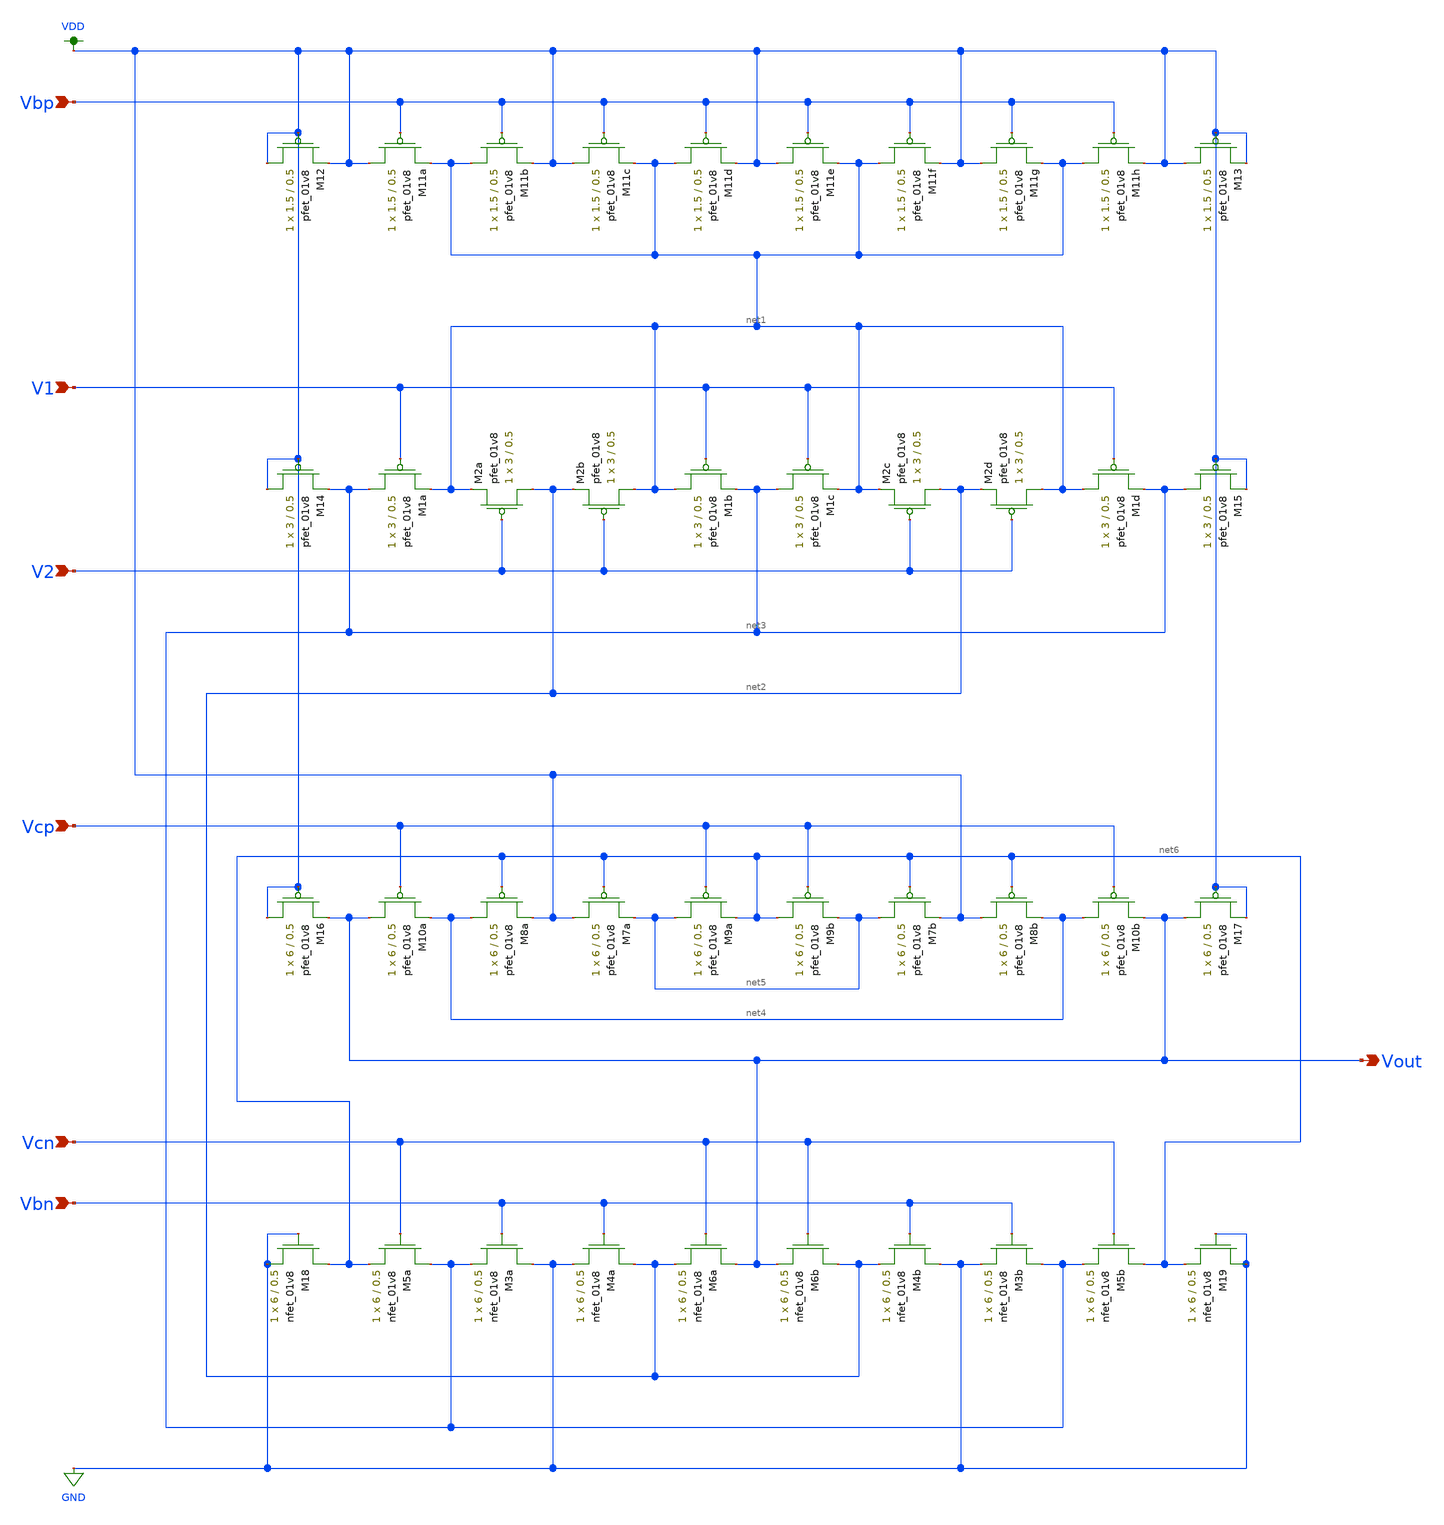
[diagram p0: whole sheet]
** sch_path: schematic/lvs_schematic/differential_pair_xschem.sch
**.subckt differential_pair_xschem Vbn Vcn Vcp V2 V1 Vbp Vout
*.ipin Vbn
*.ipin Vcn
*.ipin Vcp
*.ipin V2
*.ipin V1
*.ipin Vbp
*.opin Vout
XM5a net3 Vcn net6 GND sky130_fd_pr__nfet_01v8 L=0.5 W=6 nf=1 ad='int((nf+1)/2) * W/nf * 0.29' as='int((nf+2)/2) * W/nf * 0.29'
+ pd='2*int((nf+1)/2) * (W/nf + 0.29)' ps='2*int((nf+2)/2) * (W/nf + 0.29)' nrd='0.29 / W' nrs='0.29 / W'
+ sa=0 sb=0 sd=0 mult=1 m=1
XM1a net3 V1 net1 VDD sky130_fd_pr__pfet_01v8 L=0.5 W=3 nf=1 ad='int((nf+1)/2) * W/nf * 0.29' as='int((nf+2)/2) * W/nf * 0.29'
+ pd='2*int((nf+1)/2) * (W/nf + 0.29)' ps='2*int((nf+2)/2) * (W/nf + 0.29)' nrd='0.29 / W' nrs='0.29 / W'
+ sa=0 sb=0 sd=0 mult=1 m=1
XM2a net2 V2 net1 VDD sky130_fd_pr__pfet_01v8 L=0.5 W=3 nf=1 ad='int((nf+1)/2) * W/nf * 0.29' as='int((nf+2)/2) * W/nf * 0.29'
+ pd='2*int((nf+1)/2) * (W/nf + 0.29)' ps='2*int((nf+2)/2) * (W/nf + 0.29)' nrd='0.29 / W' nrs='0.29 / W'
+ sa=0 sb=0 sd=0 mult=1 m=1
XM2b net1 V2 net2 VDD sky130_fd_pr__pfet_01v8 L=0.5 W=3 nf=1 ad='int((nf+1)/2) * W/nf * 0.29' as='int((nf+2)/2) * W/nf * 0.29'
+ pd='2*int((nf+1)/2) * (W/nf + 0.29)' ps='2*int((nf+2)/2) * (W/nf + 0.29)' nrd='0.29 / W' nrs='0.29 / W'
+ sa=0 sb=0 sd=0 mult=1 m=1
XM1b net1 V1 net3 VDD sky130_fd_pr__pfet_01v8 L=0.5 W=3 nf=1 ad='int((nf+1)/2) * W/nf * 0.29' as='int((nf+2)/2) * W/nf * 0.29'
+ pd='2*int((nf+1)/2) * (W/nf + 0.29)' ps='2*int((nf+2)/2) * (W/nf + 0.29)' nrd='0.29 / W' nrs='0.29 / W'
+ sa=0 sb=0 sd=0 mult=1 m=1
XM1c net3 V1 net1 VDD sky130_fd_pr__pfet_01v8 L=0.5 W=3 nf=1 ad='int((nf+1)/2) * W/nf * 0.29' as='int((nf+2)/2) * W/nf * 0.29'
+ pd='2*int((nf+1)/2) * (W/nf + 0.29)' ps='2*int((nf+2)/2) * (W/nf + 0.29)' nrd='0.29 / W' nrs='0.29 / W'
+ sa=0 sb=0 sd=0 mult=1 m=1
XM2c net2 V2 net1 VDD sky130_fd_pr__pfet_01v8 L=0.5 W=3 nf=1 ad='int((nf+1)/2) * W/nf * 0.29' as='int((nf+2)/2) * W/nf * 0.29'
+ pd='2*int((nf+1)/2) * (W/nf + 0.29)' ps='2*int((nf+2)/2) * (W/nf + 0.29)' nrd='0.29 / W' nrs='0.29 / W'
+ sa=0 sb=0 sd=0 mult=1 m=1
XM2d net1 V2 net2 VDD sky130_fd_pr__pfet_01v8 L=0.5 W=3 nf=1 ad='int((nf+1)/2) * W/nf * 0.29' as='int((nf+2)/2) * W/nf * 0.29'
+ pd='2*int((nf+1)/2) * (W/nf + 0.29)' ps='2*int((nf+2)/2) * (W/nf + 0.29)' nrd='0.29 / W' nrs='0.29 / W'
+ sa=0 sb=0 sd=0 mult=1 m=1
XM1d net1 V1 net3 VDD sky130_fd_pr__pfet_01v8 L=0.5 W=3 nf=1 ad='int((nf+1)/2) * W/nf * 0.29' as='int((nf+2)/2) * W/nf * 0.29'
+ pd='2*int((nf+1)/2) * (W/nf + 0.29)' ps='2*int((nf+2)/2) * (W/nf + 0.29)' nrd='0.29 / W' nrs='0.29 / W'
+ sa=0 sb=0 sd=0 mult=1 m=1
XM11a VDD Vbp net1 VDD sky130_fd_pr__pfet_01v8 L=0.5 W=1.5 nf=1 ad='int((nf+1)/2) * W/nf * 0.29' as='int((nf+2)/2) * W/nf * 0.29'
+ pd='2*int((nf+1)/2) * (W/nf + 0.29)' ps='2*int((nf+2)/2) * (W/nf + 0.29)' nrd='0.29 / W' nrs='0.29 / W'
+ sa=0 sb=0 sd=0 mult=1 m=1
XM11b net1 Vbp VDD VDD sky130_fd_pr__pfet_01v8 L=0.5 W=1.5 nf=1 ad='int((nf+1)/2) * W/nf * 0.29' as='int((nf+2)/2) * W/nf * 0.29'
+ pd='2*int((nf+1)/2) * (W/nf + 0.29)' ps='2*int((nf+2)/2) * (W/nf + 0.29)' nrd='0.29 / W' nrs='0.29 / W'
+ sa=0 sb=0 sd=0 mult=1 m=1
XM11c VDD Vbp net1 VDD sky130_fd_pr__pfet_01v8 L=0.5 W=1.5 nf=1 ad='int((nf+1)/2) * W/nf * 0.29' as='int((nf+2)/2) * W/nf * 0.29'
+ pd='2*int((nf+1)/2) * (W/nf + 0.29)' ps='2*int((nf+2)/2) * (W/nf + 0.29)' nrd='0.29 / W' nrs='0.29 / W'
+ sa=0 sb=0 sd=0 mult=1 m=1
XM11d net1 Vbp VDD VDD sky130_fd_pr__pfet_01v8 L=0.5 W=1.5 nf=1 ad='int((nf+1)/2) * W/nf * 0.29' as='int((nf+2)/2) * W/nf * 0.29'
+ pd='2*int((nf+1)/2) * (W/nf + 0.29)' ps='2*int((nf+2)/2) * (W/nf + 0.29)' nrd='0.29 / W' nrs='0.29 / W'
+ sa=0 sb=0 sd=0 mult=1 m=1
XM11e VDD Vbp net1 VDD sky130_fd_pr__pfet_01v8 L=0.5 W=1.5 nf=1 ad='int((nf+1)/2) * W/nf * 0.29' as='int((nf+2)/2) * W/nf * 0.29'
+ pd='2*int((nf+1)/2) * (W/nf + 0.29)' ps='2*int((nf+2)/2) * (W/nf + 0.29)' nrd='0.29 / W' nrs='0.29 / W'
+ sa=0 sb=0 sd=0 mult=1 m=1
XM11f net1 Vbp VDD VDD sky130_fd_pr__pfet_01v8 L=0.5 W=1.5 nf=1 ad='int((nf+1)/2) * W/nf * 0.29' as='int((nf+2)/2) * W/nf * 0.29'
+ pd='2*int((nf+1)/2) * (W/nf + 0.29)' ps='2*int((nf+2)/2) * (W/nf + 0.29)' nrd='0.29 / W' nrs='0.29 / W'
+ sa=0 sb=0 sd=0 mult=1 m=1
XM11g VDD Vbp net1 VDD sky130_fd_pr__pfet_01v8 L=0.5 W=1.5 nf=1 ad='int((nf+1)/2) * W/nf * 0.29' as='int((nf+2)/2) * W/nf * 0.29'
+ pd='2*int((nf+1)/2) * (W/nf + 0.29)' ps='2*int((nf+2)/2) * (W/nf + 0.29)' nrd='0.29 / W' nrs='0.29 / W'
+ sa=0 sb=0 sd=0 mult=1 m=1
XM11h net1 Vbp VDD VDD sky130_fd_pr__pfet_01v8 L=0.5 W=1.5 nf=1 ad='int((nf+1)/2) * W/nf * 0.29' as='int((nf+2)/2) * W/nf * 0.29'
+ pd='2*int((nf+1)/2) * (W/nf + 0.29)' ps='2*int((nf+2)/2) * (W/nf + 0.29)' nrd='0.29 / W' nrs='0.29 / W'
+ sa=0 sb=0 sd=0 mult=1 m=1
XM3a GND Vbn net3 GND sky130_fd_pr__nfet_01v8 L=0.5 W=6 nf=1 ad='int((nf+1)/2) * W/nf * 0.29' as='int((nf+2)/2) * W/nf * 0.29'
+ pd='2*int((nf+1)/2) * (W/nf + 0.29)' ps='2*int((nf+2)/2) * (W/nf + 0.29)' nrd='0.29 / W' nrs='0.29 / W'
+ sa=0 sb=0 sd=0 mult=1 m=1
XM4a net2 Vbn GND GND sky130_fd_pr__nfet_01v8 L=0.5 W=6 nf=1 ad='int((nf+1)/2) * W/nf * 0.29' as='int((nf+2)/2) * W/nf * 0.29'
+ pd='2*int((nf+1)/2) * (W/nf + 0.29)' ps='2*int((nf+2)/2) * (W/nf + 0.29)' nrd='0.29 / W' nrs='0.29 / W'
+ sa=0 sb=0 sd=0 mult=1 m=1
XM6a Vout Vcn net2 GND sky130_fd_pr__nfet_01v8 L=0.5 W=6 nf=1 ad='int((nf+1)/2) * W/nf * 0.29' as='int((nf+2)/2) * W/nf * 0.29'
+ pd='2*int((nf+1)/2) * (W/nf + 0.29)' ps='2*int((nf+2)/2) * (W/nf + 0.29)' nrd='0.29 / W' nrs='0.29 / W'
+ sa=0 sb=0 sd=0 mult=1 m=1
XM6b net2 Vcn Vout GND sky130_fd_pr__nfet_01v8 L=0.5 W=6 nf=1 ad='int((nf+1)/2) * W/nf * 0.29' as='int((nf+2)/2) * W/nf * 0.29'
+ pd='2*int((nf+1)/2) * (W/nf + 0.29)' ps='2*int((nf+2)/2) * (W/nf + 0.29)' nrd='0.29 / W' nrs='0.29 / W'
+ sa=0 sb=0 sd=0 mult=1 m=1
XM4b GND Vbn net2 GND sky130_fd_pr__nfet_01v8 L=0.5 W=6 nf=1 ad='int((nf+1)/2) * W/nf * 0.29' as='int((nf+2)/2) * W/nf * 0.29'
+ pd='2*int((nf+1)/2) * (W/nf + 0.29)' ps='2*int((nf+2)/2) * (W/nf + 0.29)' nrd='0.29 / W' nrs='0.29 / W'
+ sa=0 sb=0 sd=0 mult=1 m=1
XM3b net3 Vbn GND GND sky130_fd_pr__nfet_01v8 L=0.5 W=6 nf=1 ad='int((nf+1)/2) * W/nf * 0.29' as='int((nf+2)/2) * W/nf * 0.29'
+ pd='2*int((nf+1)/2) * (W/nf + 0.29)' ps='2*int((nf+2)/2) * (W/nf + 0.29)' nrd='0.29 / W' nrs='0.29 / W'
+ sa=0 sb=0 sd=0 mult=1 m=1
XM5b net6 Vcn net3 GND sky130_fd_pr__nfet_01v8 L=0.5 W=6 nf=1 ad='int((nf+1)/2) * W/nf * 0.29' as='int((nf+2)/2) * W/nf * 0.29'
+ pd='2*int((nf+1)/2) * (W/nf + 0.29)' ps='2*int((nf+2)/2) * (W/nf + 0.29)' nrd='0.29 / W' nrs='0.29 / W'
+ sa=0 sb=0 sd=0 mult=1 m=1
XM10a Vout Vcp net4 VDD sky130_fd_pr__pfet_01v8 L=0.5 W=6 nf=1 ad='int((nf+1)/2) * W/nf * 0.29' as='int((nf+2)/2) * W/nf * 0.29'
+ pd='2*int((nf+1)/2) * (W/nf + 0.29)' ps='2*int((nf+2)/2) * (W/nf + 0.29)' nrd='0.29 / W' nrs='0.29 / W'
+ sa=0 sb=0 sd=0 mult=1 m=1
XM8a net4 net6 VDD VDD sky130_fd_pr__pfet_01v8 L=0.5 W=6 nf=1 ad='int((nf+1)/2) * W/nf * 0.29' as='int((nf+2)/2) * W/nf * 0.29'
+ pd='2*int((nf+1)/2) * (W/nf + 0.29)' ps='2*int((nf+2)/2) * (W/nf + 0.29)' nrd='0.29 / W' nrs='0.29 / W'
+ sa=0 sb=0 sd=0 mult=1 m=1
XM7a VDD net6 net5 VDD sky130_fd_pr__pfet_01v8 L=0.5 W=6 nf=1 ad='int((nf+1)/2) * W/nf * 0.29' as='int((nf+2)/2) * W/nf * 0.29'
+ pd='2*int((nf+1)/2) * (W/nf + 0.29)' ps='2*int((nf+2)/2) * (W/nf + 0.29)' nrd='0.29 / W' nrs='0.29 / W'
+ sa=0 sb=0 sd=0 mult=1 m=1
XM9a net5 Vcp net6 VDD sky130_fd_pr__pfet_01v8 L=0.5 W=6 nf=1 ad='int((nf+1)/2) * W/nf * 0.29' as='int((nf+2)/2) * W/nf * 0.29'
+ pd='2*int((nf+1)/2) * (W/nf + 0.29)' ps='2*int((nf+2)/2) * (W/nf + 0.29)' nrd='0.29 / W' nrs='0.29 / W'
+ sa=0 sb=0 sd=0 mult=1 m=1
XM9b net6 Vcp net5 VDD sky130_fd_pr__pfet_01v8 L=0.5 W=6 nf=1 ad='int((nf+1)/2) * W/nf * 0.29' as='int((nf+2)/2) * W/nf * 0.29'
+ pd='2*int((nf+1)/2) * (W/nf + 0.29)' ps='2*int((nf+2)/2) * (W/nf + 0.29)' nrd='0.29 / W' nrs='0.29 / W'
+ sa=0 sb=0 sd=0 mult=1 m=1
XM7b net5 net6 VDD VDD sky130_fd_pr__pfet_01v8 L=0.5 W=6 nf=1 ad='int((nf+1)/2) * W/nf * 0.29' as='int((nf+2)/2) * W/nf * 0.29'
+ pd='2*int((nf+1)/2) * (W/nf + 0.29)' ps='2*int((nf+2)/2) * (W/nf + 0.29)' nrd='0.29 / W' nrs='0.29 / W'
+ sa=0 sb=0 sd=0 mult=1 m=1
XM8b VDD net6 net4 VDD sky130_fd_pr__pfet_01v8 L=0.5 W=6 nf=1 ad='int((nf+1)/2) * W/nf * 0.29' as='int((nf+2)/2) * W/nf * 0.29'
+ pd='2*int((nf+1)/2) * (W/nf + 0.29)' ps='2*int((nf+2)/2) * (W/nf + 0.29)' nrd='0.29 / W' nrs='0.29 / W'
+ sa=0 sb=0 sd=0 mult=1 m=1
XM10b net4 Vcp Vout VDD sky130_fd_pr__pfet_01v8 L=0.5 W=6 nf=1 ad='int((nf+1)/2) * W/nf * 0.29' as='int((nf+2)/2) * W/nf * 0.29'
+ pd='2*int((nf+1)/2) * (W/nf + 0.29)' ps='2*int((nf+2)/2) * (W/nf + 0.29)' nrd='0.29 / W' nrs='0.29 / W'
+ sa=0 sb=0 sd=0 mult=1 m=1
XM15 net3 VDD VDD VDD sky130_fd_pr__pfet_01v8 L=0.5 W=3 nf=1 ad='int((nf+1)/2) * W/nf * 0.29' as='int((nf+2)/2) * W/nf * 0.29'
+ pd='2*int((nf+1)/2) * (W/nf + 0.29)' ps='2*int((nf+2)/2) * (W/nf + 0.29)' nrd='0.29 / W' nrs='0.29 / W'
+ sa=0 sb=0 sd=0 mult=1 m=1
XM14 VDD VDD net3 VDD sky130_fd_pr__pfet_01v8 L=0.5 W=3 nf=1 ad='int((nf+1)/2) * W/nf * 0.29' as='int((nf+2)/2) * W/nf * 0.29'
+ pd='2*int((nf+1)/2) * (W/nf + 0.29)' ps='2*int((nf+2)/2) * (W/nf + 0.29)' nrd='0.29 / W' nrs='0.29 / W'
+ sa=0 sb=0 sd=0 mult=1 m=1
XM13 VDD VDD VDD VDD sky130_fd_pr__pfet_01v8 L=0.5 W=1.5 nf=1 ad='int((nf+1)/2) * W/nf * 0.29' as='int((nf+2)/2) * W/nf * 0.29'
+ pd='2*int((nf+1)/2) * (W/nf + 0.29)' ps='2*int((nf+2)/2) * (W/nf + 0.29)' nrd='0.29 / W' nrs='0.29 / W'
+ sa=0 sb=0 sd=0 mult=1 m=1
XM12 VDD VDD VDD VDD sky130_fd_pr__pfet_01v8 L=0.5 W=1.5 nf=1 ad='int((nf+1)/2) * W/nf * 0.29' as='int((nf+2)/2) * W/nf * 0.29'
+ pd='2*int((nf+1)/2) * (W/nf + 0.29)' ps='2*int((nf+2)/2) * (W/nf + 0.29)' nrd='0.29 / W' nrs='0.29 / W'
+ sa=0 sb=0 sd=0 mult=1 m=1
XM16 VDD VDD Vout VDD sky130_fd_pr__pfet_01v8 L=0.5 W=6 nf=1 ad='int((nf+1)/2) * W/nf * 0.29' as='int((nf+2)/2) * W/nf * 0.29'
+ pd='2*int((nf+1)/2) * (W/nf + 0.29)' ps='2*int((nf+2)/2) * (W/nf + 0.29)' nrd='0.29 / W' nrs='0.29 / W'
+ sa=0 sb=0 sd=0 mult=1 m=1
XM17 Vout VDD VDD VDD sky130_fd_pr__pfet_01v8 L=0.5 W=6 nf=1 ad='int((nf+1)/2) * W/nf * 0.29' as='int((nf+2)/2) * W/nf * 0.29'
+ pd='2*int((nf+1)/2) * (W/nf + 0.29)' ps='2*int((nf+2)/2) * (W/nf + 0.29)' nrd='0.29 / W' nrs='0.29 / W'
+ sa=0 sb=0 sd=0 mult=1 m=1
XM19 GND GND net6 GND sky130_fd_pr__nfet_01v8 L=0.5 W=6 nf=1 ad='int((nf+1)/2) * W/nf * 0.29' as='int((nf+2)/2) * W/nf * 0.29'
+ pd='2*int((nf+1)/2) * (W/nf + 0.29)' ps='2*int((nf+2)/2) * (W/nf + 0.29)' nrd='0.29 / W' nrs='0.29 / W'
+ sa=0 sb=0 sd=0 mult=1 m=1
XM18 net6 GND GND GND sky130_fd_pr__nfet_01v8 L=0.5 W=6 nf=1 ad='int((nf+1)/2) * W/nf * 0.29' as='int((nf+2)/2) * W/nf * 0.29'
+ pd='2*int((nf+1)/2) * (W/nf + 0.29)' ps='2*int((nf+2)/2) * (W/nf + 0.29)' nrd='0.29 / W' nrs='0.29 / W'
+ sa=0 sb=0 sd=0 mult=1 m=1
**.ends
.GLOBAL VDD
.GLOBAL GND
.end
